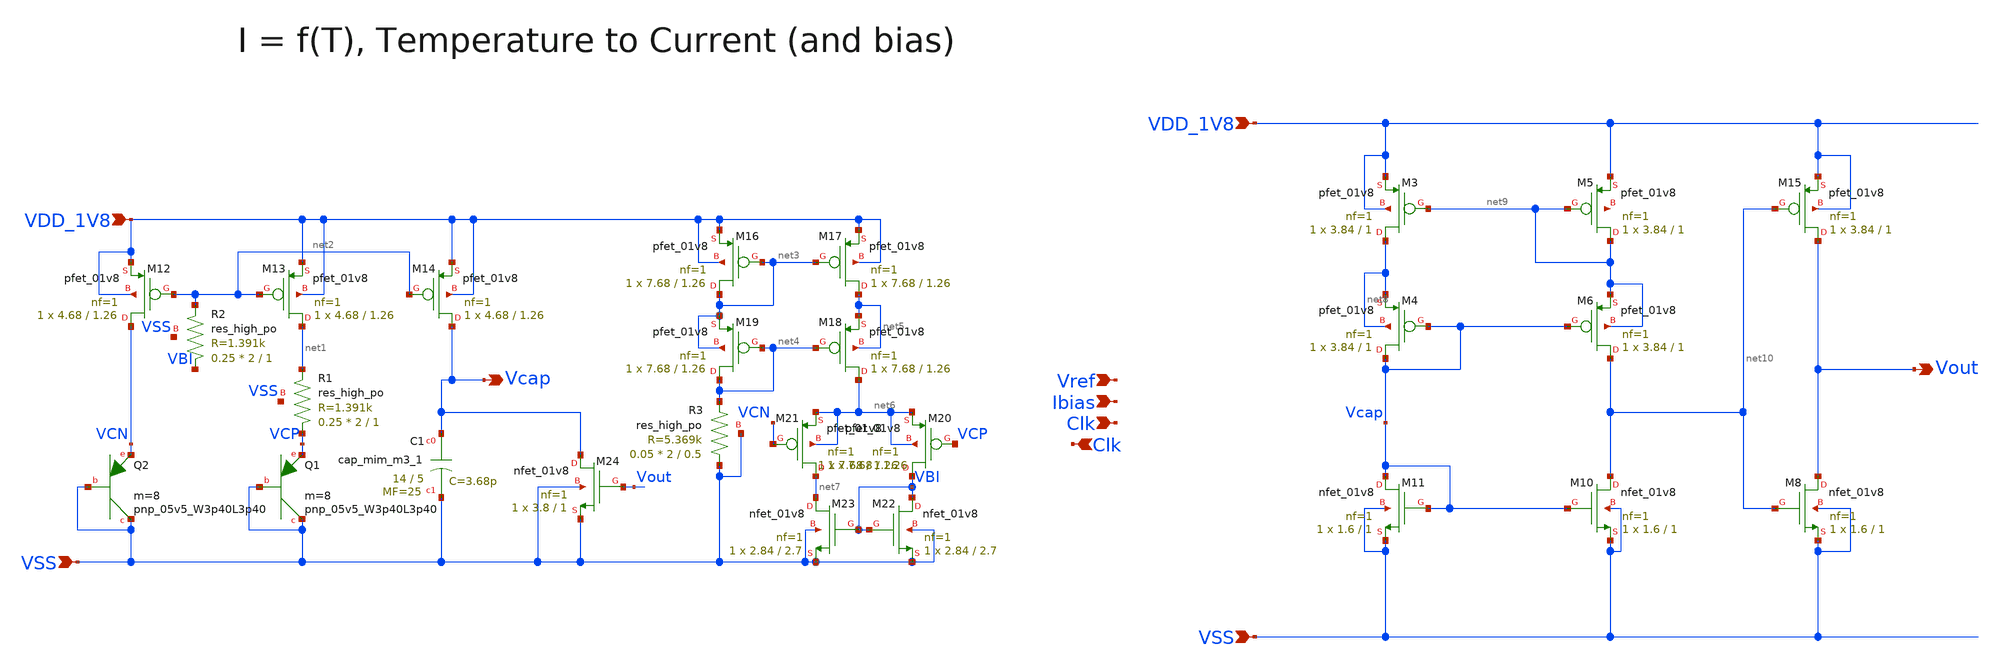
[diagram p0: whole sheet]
** sch_path: design/CNR_GR06_SKY130NM/CNR_GR06_main.sch
**.subckt CNR_GR06_main VDD_1V8 VSS Clk Vcap VDD_1V8 VSS Vref Ibias Clk Vout
*.ipin VDD_1V8
*.ipin VSS
*.ipin Clk
*.opin Vcap
*.ipin VDD_1V8
*.ipin VSS
*.ipin Vref
*.ipin Ibias
*.ipin Clk
*.opin Vout
XQ1 VSS VSS VCP sky130_fd_pr__pnp_05v5_W3p40L3p40 m=8
XR1 VCP net1 VSS sky130_fd_pr__res_high_po W=2 L=1 mult=0.25 m=0.25
XQ2 VSS VSS VCN sky130_fd_pr__pnp_05v5_W3p40L3p40 m=8
XM12 VCN net2 VDD_1V8 VDD_1V8 sky130_fd_pr__pfet_01v8 L=1.26 W=4.68 nf=1 ad='int((nf+1)/2) * W/nf * 0.29'
+ as='int((nf+2)/2) * W/nf * 0.29' pd='2*int((nf+1)/2) * (W/nf + 0.29)' ps='2*int((nf+2)/2) * (W/nf + 0.29)'
+ nrd='0.29 / W' nrs='0.29 / W' sa=0 sb=0 sd=0 mult=1 m=1
XM13 net1 net2 VDD_1V8 VDD_1V8 sky130_fd_pr__pfet_01v8 L=1.26 W=4.68 nf=1 ad='int((nf+1)/2) * W/nf * 0.29'
+ as='int((nf+2)/2) * W/nf * 0.29' pd='2*int((nf+1)/2) * (W/nf + 0.29)' ps='2*int((nf+2)/2) * (W/nf + 0.29)'
+ nrd='0.29 / W' nrs='0.29 / W' sa=0 sb=0 sd=0 mult=1 m=1
XM14 Vcap net2 VDD_1V8 VDD_1V8 sky130_fd_pr__pfet_01v8 L=1.26 W=4.68 nf=1 ad='int((nf+1)/2) * W/nf * 0.29'
+ as='int((nf+2)/2) * W/nf * 0.29' pd='2*int((nf+1)/2) * (W/nf + 0.29)' ps='2*int((nf+2)/2) * (W/nf + 0.29)'
+ nrd='0.29 / W' nrs='0.29 / W' sa=0 sb=0 sd=0 mult=1 m=1
XM16 net3 net3 VDD_1V8 VDD_1V8 sky130_fd_pr__pfet_01v8 L=1.26 W=7.68 nf=1 ad='int((nf+1)/2) * W/nf * 0.29'
+ as='int((nf+2)/2) * W/nf * 0.29' pd='2*int((nf+1)/2) * (W/nf + 0.29)' ps='2*int((nf+2)/2) * (W/nf + 0.29)'
+ nrd='0.29 / W' nrs='0.29 / W' sa=0 sb=0 sd=0 mult=1 m=1
XM17 net5 net3 VDD_1V8 VDD_1V8 sky130_fd_pr__pfet_01v8 L=1.26 W=7.68 nf=1 ad='int((nf+1)/2) * W/nf * 0.29'
+ as='int((nf+2)/2) * W/nf * 0.29' pd='2*int((nf+1)/2) * (W/nf + 0.29)' ps='2*int((nf+2)/2) * (W/nf + 0.29)'
+ nrd='0.29 / W' nrs='0.29 / W' sa=0 sb=0 sd=0 mult=1 m=1
XM18 net6 net4 net5 net5 sky130_fd_pr__pfet_01v8 L=1.26 W=7.68 nf=1 ad='int((nf+1)/2) * W/nf * 0.29'
+ as='int((nf+2)/2) * W/nf * 0.29' pd='2*int((nf+1)/2) * (W/nf + 0.29)' ps='2*int((nf+2)/2) * (W/nf + 0.29)'
+ nrd='0.29 / W' nrs='0.29 / W' sa=0 sb=0 sd=0 mult=1 m=1
XM19 net4 net4 net3 net3 sky130_fd_pr__pfet_01v8 L=1.26 W=7.68 nf=1 ad='int((nf+1)/2) * W/nf * 0.29'
+ as='int((nf+2)/2) * W/nf * 0.29' pd='2*int((nf+1)/2) * (W/nf + 0.29)' ps='2*int((nf+2)/2) * (W/nf + 0.29)'
+ nrd='0.29 / W' nrs='0.29 / W' sa=0 sb=0 sd=0 mult=1 m=1
XM20 VBI VCP net6 net6 sky130_fd_pr__pfet_01v8 L=1.26 W=7.68 nf=1 ad='int((nf+1)/2) * W/nf * 0.29' as='int((nf+2)/2) * W/nf * 0.29'
+ pd='2*int((nf+1)/2) * (W/nf + 0.29)' ps='2*int((nf+2)/2) * (W/nf + 0.29)' nrd='0.29 / W' nrs='0.29 / W'
+ sa=0 sb=0 sd=0 mult=1 m=1
XM21 net7 VCN net6 net6 sky130_fd_pr__pfet_01v8 L=1.26 W=7.68 nf=1 ad='int((nf+1)/2) * W/nf * 0.29' as='int((nf+2)/2) * W/nf * 0.29'
+ pd='2*int((nf+1)/2) * (W/nf + 0.29)' ps='2*int((nf+2)/2) * (W/nf + 0.29)' nrd='0.29 / W' nrs='0.29 / W'
+ sa=0 sb=0 sd=0 mult=1 m=1
XM22 VBI VBI VSS VSS sky130_fd_pr__nfet_01v8 L=2.7 W=2.84 nf=1 ad='int((nf+1)/2) * W/nf * 0.29' as='int((nf+2)/2) * W/nf * 0.29'
+ pd='2*int((nf+1)/2) * (W/nf + 0.29)' ps='2*int((nf+2)/2) * (W/nf + 0.29)' nrd='0.29 / W' nrs='0.29 / W'
+ sa=0 sb=0 sd=0 mult=1 m=1
XM23 net7 VBI VSS VSS sky130_fd_pr__nfet_01v8 L=2.7 W=2.84 nf=1 ad='int((nf+1)/2) * W/nf * 0.29' as='int((nf+2)/2) * W/nf * 0.29'
+ pd='2*int((nf+1)/2) * (W/nf + 0.29)' ps='2*int((nf+2)/2) * (W/nf + 0.29)' nrd='0.29 / W' nrs='0.29 / W'
+ sa=0 sb=0 sd=0 mult=1 m=1
XR3 VSS net4 VSS sky130_fd_pr__res_high_po W=2 L=0.5 mult=0.05 m=0.05
XC1 Vcap VSS sky130_fd_pr__cap_mim_m3_1 W=14 L=5 MF=25 m=25
XM24 Vcap Vout VSS VSS sky130_fd_pr__nfet_01v8 L=1 W=3.8 nf=1 ad='int((nf+1)/2) * W/nf * 0.29' as='int((nf+2)/2) * W/nf * 0.29'
+ pd='2*int((nf+1)/2) * (W/nf + 0.29)' ps='2*int((nf+2)/2) * (W/nf + 0.29)' nrd='0.29 / W' nrs='0.29 / W'
+ sa=0 sb=0 sd=0 mult=1 m=1
XR2 VBI net2 VSS sky130_fd_pr__res_high_po W=2 L=1 mult=0.25 m=0.25
XM3 net8 net9 VDD_1V8 VDD_1V8 sky130_fd_pr__pfet_01v8 L=1 W=3.84 nf=1 ad='int((nf+1)/2) * W/nf * 0.29'
+ as='int((nf+2)/2) * W/nf * 0.29' pd='2*int((nf+1)/2) * (W/nf + 0.29)' ps='2*int((nf+2)/2) * (W/nf + 0.29)'
+ nrd='0.29 / W' nrs='0.29 / W' sa=0 sb=0 sd=0 mult=1 m=1
XM10 net10 Vcap VSS VSS sky130_fd_pr__nfet_01v8 L=1 W=1.6 nf=1 ad='int((nf+1)/2) * W/nf * 0.29' as='int((nf+2)/2) * W/nf * 0.29'
+ pd='2*int((nf+1)/2) * (W/nf + 0.29)' ps='2*int((nf+2)/2) * (W/nf + 0.29)' nrd='0.29 / W' nrs='0.29 / W'
+ sa=0 sb=0 sd=0 mult=1 m=1
XM11 Vcap Vcap VSS VSS sky130_fd_pr__nfet_01v8 L=1 W=1.6 nf=1 ad='int((nf+1)/2) * W/nf * 0.29' as='int((nf+2)/2) * W/nf * 0.29'
+ pd='2*int((nf+1)/2) * (W/nf + 0.29)' ps='2*int((nf+2)/2) * (W/nf + 0.29)' nrd='0.29 / W' nrs='0.29 / W'
+ sa=0 sb=0 sd=0 mult=1 m=1
XM5 net9 net9 VDD_1V8 net11 sky130_fd_pr__pfet_01v8 L=1 W=3.84 nf=1 ad='int((nf+1)/2) * W/nf * 0.29'
+ as='int((nf+2)/2) * W/nf * 0.29' pd='2*int((nf+1)/2) * (W/nf + 0.29)' ps='2*int((nf+2)/2) * (W/nf + 0.29)'
+ nrd='0.29 / W' nrs='0.29 / W' sa=0 sb=0 sd=0 mult=1 m=1
XM15 Vout net10 VDD_1V8 VDD_1V8 sky130_fd_pr__pfet_01v8 L=1 W=3.84 nf=1 ad='int((nf+1)/2) * W/nf * 0.29'
+ as='int((nf+2)/2) * W/nf * 0.29' pd='2*int((nf+1)/2) * (W/nf + 0.29)' ps='2*int((nf+2)/2) * (W/nf + 0.29)'
+ nrd='0.29 / W' nrs='0.29 / W' sa=0 sb=0 sd=0 mult=1 m=1
XM4 Vcap Vcap net8 net8 sky130_fd_pr__pfet_01v8 L=1 W=3.84 nf=1 ad='int((nf+1)/2) * W/nf * 0.29' as='int((nf+2)/2) * W/nf * 0.29'
+ pd='2*int((nf+1)/2) * (W/nf + 0.29)' ps='2*int((nf+2)/2) * (W/nf + 0.29)' nrd='0.29 / W' nrs='0.29 / W'
+ sa=0 sb=0 sd=0 mult=1 m=1
XM6 net10 Vcap net9 net9 sky130_fd_pr__pfet_01v8 L=1 W=3.84 nf=1 ad='int((nf+1)/2) * W/nf * 0.29' as='int((nf+2)/2) * W/nf * 0.29'
+ pd='2*int((nf+1)/2) * (W/nf + 0.29)' ps='2*int((nf+2)/2) * (W/nf + 0.29)' nrd='0.29 / W' nrs='0.29 / W'
+ sa=0 sb=0 sd=0 mult=1 m=1
XM8 Vout net10 VSS VSS sky130_fd_pr__nfet_01v8 L=1 W=1.6 nf=1 ad='int((nf+1)/2) * W/nf * 0.29' as='int((nf+2)/2) * W/nf * 0.29'
+ pd='2*int((nf+1)/2) * (W/nf + 0.29)' ps='2*int((nf+2)/2) * (W/nf + 0.29)' nrd='0.29 / W' nrs='0.29 / W'
+ sa=0 sb=0 sd=0 mult=1 m=1
**.ends
.end
